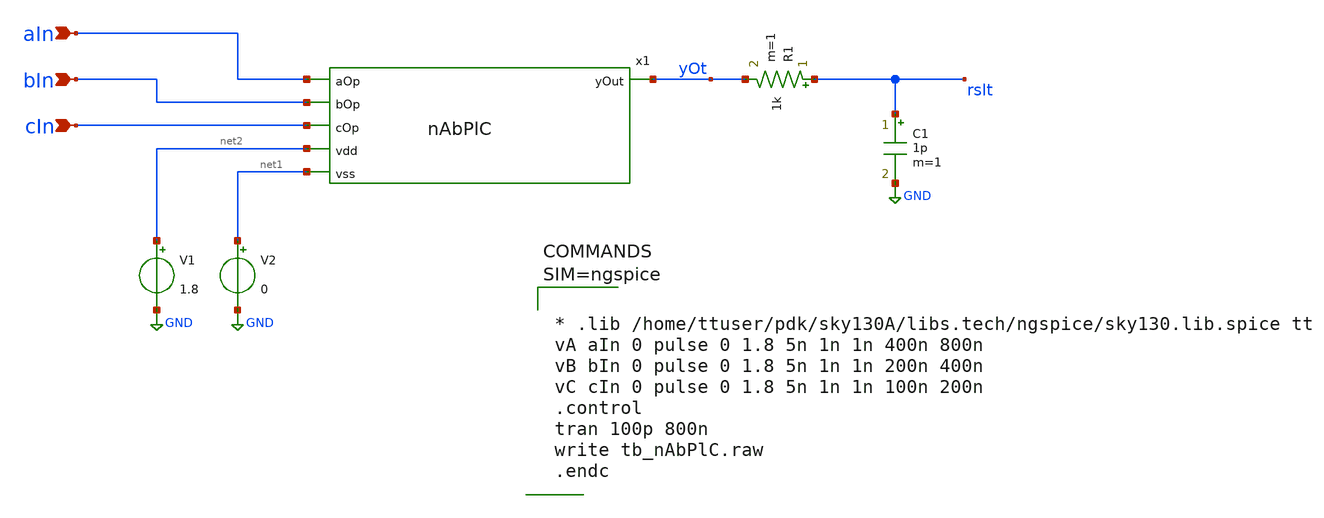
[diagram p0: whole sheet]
** sch_path: xschem/tb_nAbPlC.sch
**.subckt tb_nAbPlC bIn aIn cIn
*.ipin bIn
*.ipin aIn
*.ipin cIn
x1 aIn bIn cIn net2 yOt net1 nAbPlC
R1 rslt yOt 1k m=1
C1 rslt GND 1p m=1
V1 net2 GND 1.8
V2 net1 GND 0
**** begin user architecture code

** opencircuitdesign pdks install
.lib $::SKYWATER_MODELS/sky130.lib.spice tt





* .lib /home/ttuser/pdk/sky130A/libs.tech/ngspice/sky130.lib.spice tt
vA aIn 0 pulse 0 1.8 5n 1n 1n 400n 800n
vB bIn 0 pulse 0 1.8 5n 1n 1n 200n 400n
vC cIn 0 pulse 0 1.8 5n 1n 1n 100n 200n
.control
tran 100p 800n
write tb_nAbPlC.raw
.endc



**** end user architecture code
**.ends

* expanding   symbol:  /home/ttuser/nAbPlC/nAbPlC.sym # of pins=6
** sym_path: xschem/nAbPlC.sym
** sch_path: xschem/nAbPlC.sch
.subckt nAbPlC aOp bOp cOp vdd yOut vss
*.ipin aOp
*.ipin bOp
*.ipin cOp
*.ipin vdd
*.ipin vss
*.opin yOut
XM1 ab_c aOp vdd VDD sky130_fd_pr__pfet_01v8 L=0.15 W=1 nf=1 ad='int((nf+1)/2) * W/nf * 0.29' as='int((nf+2)/2) * W/nf * 0.29'
+ pd='2*int((nf+1)/2) * (W/nf + 0.29)' ps='2*int((nf+2)/2) * (W/nf + 0.29)' nrd='0.29 / W' nrs='0.29 / W'
+ sa=0 sb=0 sd=0 mult=1 m=1
XM2 ab_c bOp vdd VDD sky130_fd_pr__pfet_01v8 L=0.15 W=1 nf=1 ad='int((nf+1)/2) * W/nf * 0.29' as='int((nf+2)/2) * W/nf * 0.29'
+ pd='2*int((nf+1)/2) * (W/nf + 0.29)' ps='2*int((nf+2)/2) * (W/nf + 0.29)' nrd='0.29 / W' nrs='0.29 / W'
+ sa=0 sb=0 sd=0 mult=1 m=1
XM3 yOut cOp ab_c VDD sky130_fd_pr__pfet_01v8 L=0.15 W=1 nf=1 ad='int((nf+1)/2) * W/nf * 0.29' as='int((nf+2)/2) * W/nf * 0.29'
+ pd='2*int((nf+1)/2) * (W/nf + 0.29)' ps='2*int((nf+2)/2) * (W/nf + 0.29)' nrd='0.29 / W' nrs='0.29 / W'
+ sa=0 sb=0 sd=0 mult=1 m=1
XM4 yOut aOp a_b GND sky130_fd_pr__nfet_01v8 L=0.15 W=1 nf=1 ad='int((nf+1)/2) * W/nf * 0.29' as='int((nf+2)/2) * W/nf * 0.29'
+ pd='2*int((nf+1)/2) * (W/nf + 0.29)' ps='2*int((nf+2)/2) * (W/nf + 0.29)' nrd='0.29 / W' nrs='0.29 / W'
+ sa=0 sb=0 sd=0 mult=1 m=1
XM5 a_b bOp vss GND sky130_fd_pr__nfet_01v8 L=0.15 W=1 nf=1 ad='int((nf+1)/2) * W/nf * 0.29' as='int((nf+2)/2) * W/nf * 0.29'
+ pd='2*int((nf+1)/2) * (W/nf + 0.29)' ps='2*int((nf+2)/2) * (W/nf + 0.29)' nrd='0.29 / W' nrs='0.29 / W'
+ sa=0 sb=0 sd=0 mult=1 m=1
XM6 yOut cOp vss GND sky130_fd_pr__nfet_01v8 L=0.15 W=1 nf=1 ad='int((nf+1)/2) * W/nf * 0.29' as='int((nf+2)/2) * W/nf * 0.29'
+ pd='2*int((nf+1)/2) * (W/nf + 0.29)' ps='2*int((nf+2)/2) * (W/nf + 0.29)' nrd='0.29 / W' nrs='0.29 / W'
+ sa=0 sb=0 sd=0 mult=1 m=1
.ends

.GLOBAL GND
.end
